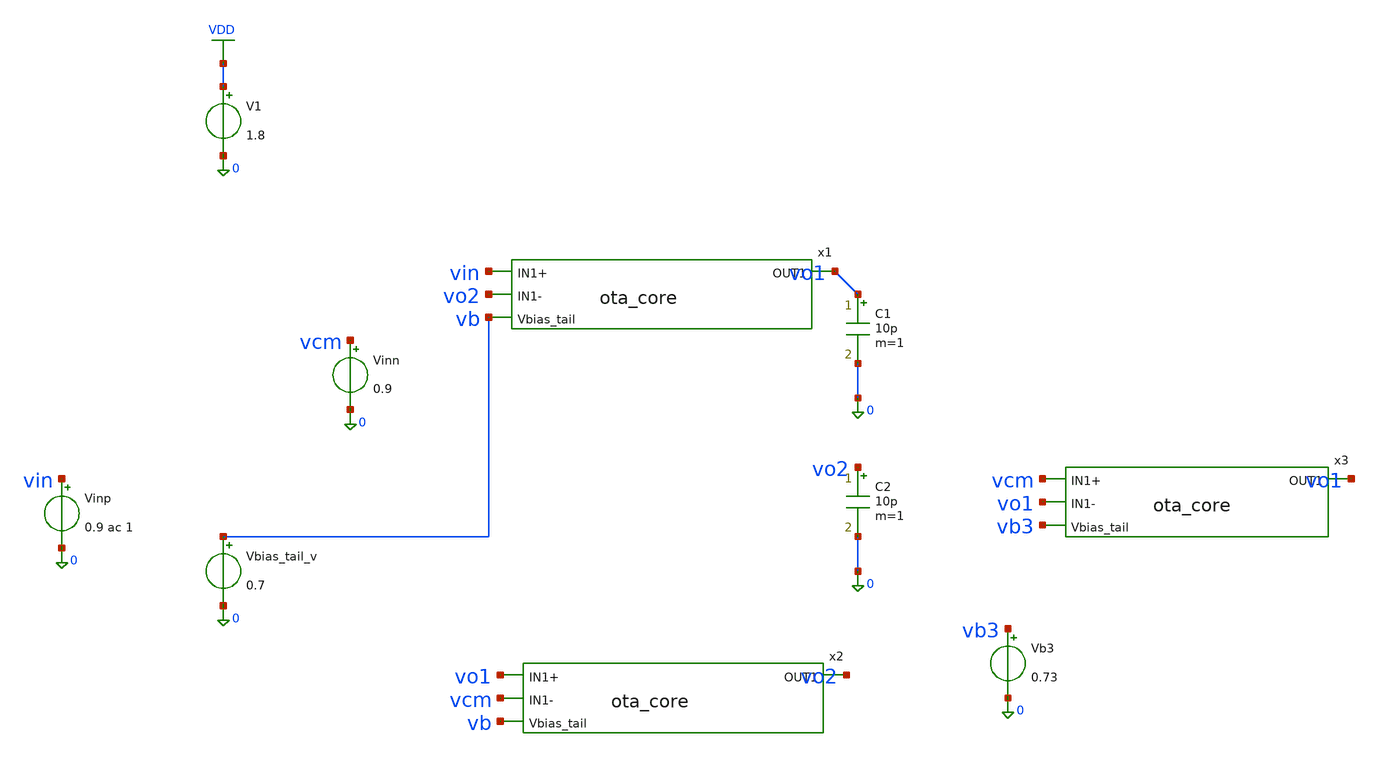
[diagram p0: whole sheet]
** sch_path: gmc_top.sch
**.subckt gmc_top
Vinp vin 0 0.9 ac 1
V1 VDD 0 1.8
Vinn vcm 0 0.9
Vbias_tail_v vb 0 0.7
C1 vo1 0 10p m=1
x1 vo1 vin vo2 vb ota_core
x2 vo2 vo1 vcm vb ota_core
x3 vo1 vcm vo1 vb3 ota_core
C2 vo2 0 10p m=1
Vb3 vb3 0 0.73
**** begin user architecture code

.lib /foss/pdks/sky130A/libs.tech/combined/sky130.lib.spice tt_mm


.include /foss/designs/gmc-filter/mc_run.cir

**** end user architecture code
**.ends

* expanding   symbol:  ota_core.sym # of pins=4
** sym_path: ota_core.sym
** sch_path: ota_core.sch
.subckt ota_core OUT1 IN1+ IN1- Vbias_tail
*.ipin IN1+
*.ipin IN1-
*.opin OUT1
*.ipin Vbias_tail
XM1 net2 IN1+ net1 0 sky130_fd_pr__nfet_01v8 L=0.5 W=4 nf=1 ad='int((1 + 1)/2) * 4 / 1 * 0.29' as='int((1 + 2)/2) * 4 / 1 * 0.29'
+ pd='2*int((1 + 1)/2) * (4 / 1 + 0.29)' ps='2*int((1 + 2)/2) * (4 / 1 + 0.29)' nrd='0.29 / 4 ' nrs='0.29 / 4 '
+ sa=0 sb=0 sd=0 mult=1 m=1
XM2 OUT1 IN1- net1 0 sky130_fd_pr__nfet_01v8 L=0.5 W=4 nf=1 ad='int((1 + 1)/2) * 4 / 1 * 0.29' as='int((1 + 2)/2) * 4 / 1 * 0.29'
+ pd='2*int((1 + 1)/2) * (4 / 1 + 0.29)' ps='2*int((1 + 2)/2) * (4 / 1 + 0.29)' nrd='0.29 / 4 ' nrs='0.29 / 4 '
+ sa=0 sb=0 sd=0 mult=1 m=1
XM3 net2 net2 VDD VDD sky130_fd_pr__pfet_01v8 L=0.5 W=8 nf=1 ad='int((1 + 1)/2) * 8 / 1 * 0.29' as='int((1 + 2)/2) * 8 / 1 * 0.29'
+ pd='2*int((1 + 1)/2) * (8 / 1 + 0.29)' ps='2*int((1 + 2)/2) * (8 / 1 + 0.29)' nrd='0.29 / 8 ' nrs='0.29 / 8 '
+ sa=0 sb=0 sd=0 mult=1 m=1
XM4 OUT1 net2 VDD VDD sky130_fd_pr__pfet_01v8 L=0.5 W=8 nf=1 ad='int((1 + 1)/2) * 8 / 1 * 0.29' as='int((1 + 2)/2) * 8 / 1 * 0.29'
+ pd='2*int((1 + 1)/2) * (8 / 1 + 0.29)' ps='2*int((1 + 2)/2) * (8 / 1 + 0.29)' nrd='0.29 / 8 ' nrs='0.29 / 8 '
+ sa=0 sb=0 sd=0 mult=1 m=1
XM5 net1 Vbias_tail 0 0 sky130_fd_pr__nfet_01v8 L=1 W=6 nf=1 ad='int((1 + 1)/2) * 6 / 1 * 0.29' as='int((1 + 2)/2) * 6 / 1 * 0.29'
+ pd='2*int((1 + 1)/2) * (6 / 1 + 0.29)' ps='2*int((1 + 2)/2) * (6 / 1 + 0.29)' nrd='0.29 / 6 ' nrs='0.29 / 6 '
+ sa=0 sb=0 sd=0 mult=1 m=1
.ends

.GLOBAL VDD
.end
